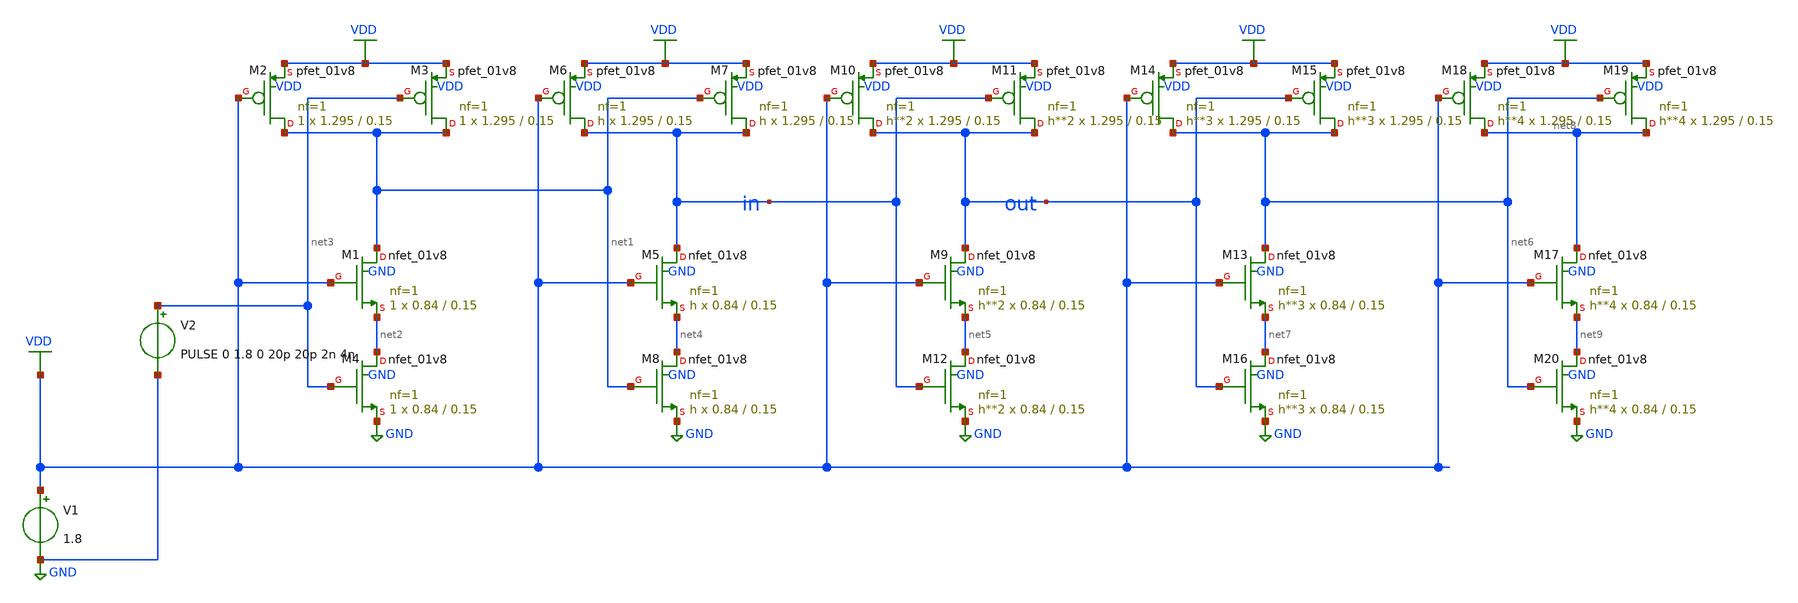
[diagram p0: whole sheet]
** sch_path: static_cmos/logicaleffort/nand2_b.sch
**.subckt nand2_b
XM1 net1 VDD net2 GND sky130_fd_pr__nfet_01v8 L=0.15 W=0.84 nf=1 ad='int((1 + 1)/2) * 0.84 / 1 * 0.29'
+ as='int((1 + 2)/2) * 0.84 / 1 * 0.29' pd='2*int((1 + 1)/2) * (0.84 / 1 + 0.29)' ps='2*int((1 + 2)/2) * (0.84 / 1 + 0.29)'
+ nrd='0.29 / 0.84 ' nrs='0.29 / 0.84 ' sa=0 sb=0 sd=0 mult=1 m=1
XM2 net1 VDD VDD VDD sky130_fd_pr__pfet_01v8 L=0.15 W=1.295 nf=1 ad='int((1 + 1)/2) * 1.295 / 1 * 0.29'
+ as='int((1 + 2)/2) * 1.295 / 1 * 0.29' pd='2*int((1 + 1)/2) * (1.295 / 1 + 0.29)' ps='2*int((1 + 2)/2) * (1.295 / 1 + 0.29)'
+ nrd='0.29 / 1.295 ' nrs='0.29 / 1.295 ' sa=0 sb=0 sd=0 mult=1 m=1
XM3 net1 net3 VDD VDD sky130_fd_pr__pfet_01v8 L=0.15 W=1.295 nf=1 ad='int((1 + 1)/2) * 1.295 / 1 * 0.29'
+ as='int((1 + 2)/2) * 1.295 / 1 * 0.29' pd='2*int((1 + 1)/2) * (1.295 / 1 + 0.29)' ps='2*int((1 + 2)/2) * (1.295 / 1 + 0.29)'
+ nrd='0.29 / 1.295 ' nrs='0.29 / 1.295 ' sa=0 sb=0 sd=0 mult=1 m=1
XM4 net2 net3 GND GND sky130_fd_pr__nfet_01v8 L=0.15 W=0.84 nf=1 ad='int((1 + 1)/2) * 0.84 / 1 * 0.29'
+ as='int((1 + 2)/2) * 0.84 / 1 * 0.29' pd='2*int((1 + 1)/2) * (0.84 / 1 + 0.29)' ps='2*int((1 + 2)/2) * (0.84 / 1 + 0.29)'
+ nrd='0.29 / 0.84 ' nrs='0.29 / 0.84 ' sa=0 sb=0 sd=0 mult=1 m=1
XM5 in VDD net4 GND sky130_fd_pr__nfet_01v8 L=0.15 W=0.84 nf=1 ad='int((1 + 1)/2) * 0.84 / 1 * 0.29'
+ as='int((1 + 2)/2) * 0.84 / 1 * 0.29' pd='2*int((1 + 1)/2) * (0.84 / 1 + 0.29)' ps='2*int((1 + 2)/2) * (0.84 / 1 + 0.29)'
+ nrd='0.29 / 0.84 ' nrs='0.29 / 0.84 ' sa=0 sb=0 sd=0 mult=h m=h
XM6 in VDD VDD VDD sky130_fd_pr__pfet_01v8 L=0.15 W=1.295 nf=1 ad='int((1 + 1)/2) * 1.295 / 1 * 0.29'
+ as='int((1 + 2)/2) * 1.295 / 1 * 0.29' pd='2*int((1 + 1)/2) * (1.295 / 1 + 0.29)' ps='2*int((1 + 2)/2) * (1.295 / 1 + 0.29)'
+ nrd='0.29 / 1.295 ' nrs='0.29 / 1.295 ' sa=0 sb=0 sd=0 mult=h m=h
XM7 in net1 VDD VDD sky130_fd_pr__pfet_01v8 L=0.15 W=1.295 nf=1 ad='int((1 + 1)/2) * 1.295 / 1 * 0.29'
+ as='int((1 + 2)/2) * 1.295 / 1 * 0.29' pd='2*int((1 + 1)/2) * (1.295 / 1 + 0.29)' ps='2*int((1 + 2)/2) * (1.295 / 1 + 0.29)'
+ nrd='0.29 / 1.295 ' nrs='0.29 / 1.295 ' sa=0 sb=0 sd=0 mult=h m=h
XM8 net4 net1 GND GND sky130_fd_pr__nfet_01v8 L=0.15 W=0.84 nf=1 ad='int((1 + 1)/2) * 0.84 / 1 * 0.29'
+ as='int((1 + 2)/2) * 0.84 / 1 * 0.29' pd='2*int((1 + 1)/2) * (0.84 / 1 + 0.29)' ps='2*int((1 + 2)/2) * (0.84 / 1 + 0.29)'
+ nrd='0.29 / 0.84 ' nrs='0.29 / 0.84 ' sa=0 sb=0 sd=0 mult=h m=h
XM9 out VDD net5 GND sky130_fd_pr__nfet_01v8 L=0.15 W=0.84 nf=1 ad='int((1 + 1)/2) * 0.84 / 1 * 0.29'
+ as='int((1 + 2)/2) * 0.84 / 1 * 0.29' pd='2*int((1 + 1)/2) * (0.84 / 1 + 0.29)' ps='2*int((1 + 2)/2) * (0.84 / 1 + 0.29)'
+ nrd='0.29 / 0.84 ' nrs='0.29 / 0.84 ' sa=0 sb=0 sd=0 mult=h**2 m=h**2
XM10 out VDD VDD VDD sky130_fd_pr__pfet_01v8 L=0.15 W=1.295 nf=1 ad='int((1 + 1)/2) * 1.295 / 1 * 0.29'
+ as='int((1 + 2)/2) * 1.295 / 1 * 0.29' pd='2*int((1 + 1)/2) * (1.295 / 1 + 0.29)' ps='2*int((1 + 2)/2) * (1.295 / 1 + 0.29)'
+ nrd='0.29 / 1.295 ' nrs='0.29 / 1.295 ' sa=0 sb=0 sd=0 mult=h**2 m=h**2
XM11 out in VDD VDD sky130_fd_pr__pfet_01v8 L=0.15 W=1.295 nf=1 ad='int((1 + 1)/2) * 1.295 / 1 * 0.29'
+ as='int((1 + 2)/2) * 1.295 / 1 * 0.29' pd='2*int((1 + 1)/2) * (1.295 / 1 + 0.29)' ps='2*int((1 + 2)/2) * (1.295 / 1 + 0.29)'
+ nrd='0.29 / 1.295 ' nrs='0.29 / 1.295 ' sa=0 sb=0 sd=0 mult=h**2 m=h**2
XM12 net5 in GND GND sky130_fd_pr__nfet_01v8 L=0.15 W=0.84 nf=1 ad='int((1 + 1)/2) * 0.84 / 1 * 0.29'
+ as='int((1 + 2)/2) * 0.84 / 1 * 0.29' pd='2*int((1 + 1)/2) * (0.84 / 1 + 0.29)' ps='2*int((1 + 2)/2) * (0.84 / 1 + 0.29)'
+ nrd='0.29 / 0.84 ' nrs='0.29 / 0.84 ' sa=0 sb=0 sd=0 mult=h**2 m=h**2
XM13 net6 VDD net7 GND sky130_fd_pr__nfet_01v8 L=0.15 W=0.84 nf=1 ad='int((1 + 1)/2) * 0.84 / 1 * 0.29'
+ as='int((1 + 2)/2) * 0.84 / 1 * 0.29' pd='2*int((1 + 1)/2) * (0.84 / 1 + 0.29)' ps='2*int((1 + 2)/2) * (0.84 / 1 + 0.29)'
+ nrd='0.29 / 0.84 ' nrs='0.29 / 0.84 ' sa=0 sb=0 sd=0 mult=h**3 m=h**3
XM14 net6 VDD VDD VDD sky130_fd_pr__pfet_01v8 L=0.15 W=1.295 nf=1 ad='int((1 + 1)/2) * 1.295 / 1 * 0.29'
+ as='int((1 + 2)/2) * 1.295 / 1 * 0.29' pd='2*int((1 + 1)/2) * (1.295 / 1 + 0.29)' ps='2*int((1 + 2)/2) * (1.295 / 1 + 0.29)'
+ nrd='0.29 / 1.295 ' nrs='0.29 / 1.295 ' sa=0 sb=0 sd=0 mult=h**3 m=h**3
XM15 net6 out VDD VDD sky130_fd_pr__pfet_01v8 L=0.15 W=1.295 nf=1 ad='int((1 + 1)/2) * 1.295 / 1 * 0.29'
+ as='int((1 + 2)/2) * 1.295 / 1 * 0.29' pd='2*int((1 + 1)/2) * (1.295 / 1 + 0.29)' ps='2*int((1 + 2)/2) * (1.295 / 1 + 0.29)'
+ nrd='0.29 / 1.295 ' nrs='0.29 / 1.295 ' sa=0 sb=0 sd=0 mult=h**3 m=h**3
XM16 net7 out GND GND sky130_fd_pr__nfet_01v8 L=0.15 W=0.84 nf=1 ad='int((1 + 1)/2) * 0.84 / 1 * 0.29'
+ as='int((1 + 2)/2) * 0.84 / 1 * 0.29' pd='2*int((1 + 1)/2) * (0.84 / 1 + 0.29)' ps='2*int((1 + 2)/2) * (0.84 / 1 + 0.29)'
+ nrd='0.29 / 0.84 ' nrs='0.29 / 0.84 ' sa=0 sb=0 sd=0 mult=h**3 m=h**3
XM17 net8 VDD net9 GND sky130_fd_pr__nfet_01v8 L=0.15 W=0.84 nf=1 ad='int((1 + 1)/2) * 0.84 / 1 * 0.29'
+ as='int((1 + 2)/2) * 0.84 / 1 * 0.29' pd='2*int((1 + 1)/2) * (0.84 / 1 + 0.29)' ps='2*int((1 + 2)/2) * (0.84 / 1 + 0.29)'
+ nrd='0.29 / 0.84 ' nrs='0.29 / 0.84 ' sa=0 sb=0 sd=0 mult=h**4 m=h**4
XM18 net8 VDD VDD VDD sky130_fd_pr__pfet_01v8 L=0.15 W=1.295 nf=1 ad='int((1 + 1)/2) * 1.295 / 1 * 0.29'
+ as='int((1 + 2)/2) * 1.295 / 1 * 0.29' pd='2*int((1 + 1)/2) * (1.295 / 1 + 0.29)' ps='2*int((1 + 2)/2) * (1.295 / 1 + 0.29)'
+ nrd='0.29 / 1.295 ' nrs='0.29 / 1.295 ' sa=0 sb=0 sd=0 mult=h**4 m=h**4
XM19 net8 net6 VDD VDD sky130_fd_pr__pfet_01v8 L=0.15 W=1.295 nf=1 ad='int((1 + 1)/2) * 1.295 / 1 * 0.29'
+ as='int((1 + 2)/2) * 1.295 / 1 * 0.29' pd='2*int((1 + 1)/2) * (1.295 / 1 + 0.29)' ps='2*int((1 + 2)/2) * (1.295 / 1 + 0.29)'
+ nrd='0.29 / 1.295 ' nrs='0.29 / 1.295 ' sa=0 sb=0 sd=0 mult=h**4 m=h**4
XM20 net9 net6 GND GND sky130_fd_pr__nfet_01v8 L=0.15 W=0.84 nf=1 ad='int((1 + 1)/2) * 0.84 / 1 * 0.29'
+ as='int((1 + 2)/2) * 0.84 / 1 * 0.29' pd='2*int((1 + 1)/2) * (0.84 / 1 + 0.29)' ps='2*int((1 + 2)/2) * (0.84 / 1 + 0.29)'
+ nrd='0.29 / 0.84 ' nrs='0.29 / 0.84 ' sa=0 sb=0 sd=0 mult=h**4 m=h**4
V1 VDD GND 1.8
V2 net3 GND PULSE 0 1.8 0 20p 20p 2n 4n
**** begin user architecture code


.lib /usr/local/share/pdk/sky130A/libs.tech/ngspice/sky130.lib.spice tt

.param h = 4
.control
  save in out
  let start = 1
  let stop = 8
  let step = 1
  let cur = start
  let n = ((stop - start) / step) + 1
  let hall = unitvec(n)
  let tpdrall = unitvec(n)
  let tpdfall = unitvec(n)
  let tpdall = unitvec(n)
  let diffall = unitvec(n)
  let m = 0
  while m < n
    let hv = cur
    alterparam h = $&hv
    reset
    tran 0.1p 20n
    meas tran tpdr trig v(in) val=0.9 fall=1 targ v(out) val=0.9 rise=1
    meas tran tpdf trig v(in) val=0.9 rise=1 targ v(out) val=0.9 fall=1
    let hall[m] = hv
    let tpdrall[m] = tpdr
    let tpdfall[m] = tpdf
    let tpdall[m] = (tpdr + tpdf) / 2
    let diffall[m] = abs(tpdr - tpdf)
    let cur = cur + step
    let m = m + 1
  end
  print hall tpdrall tpdfall tpdall diffall
.endc


**** end user architecture code
**.ends
.GLOBAL GND
.GLOBAL VDD
.end
